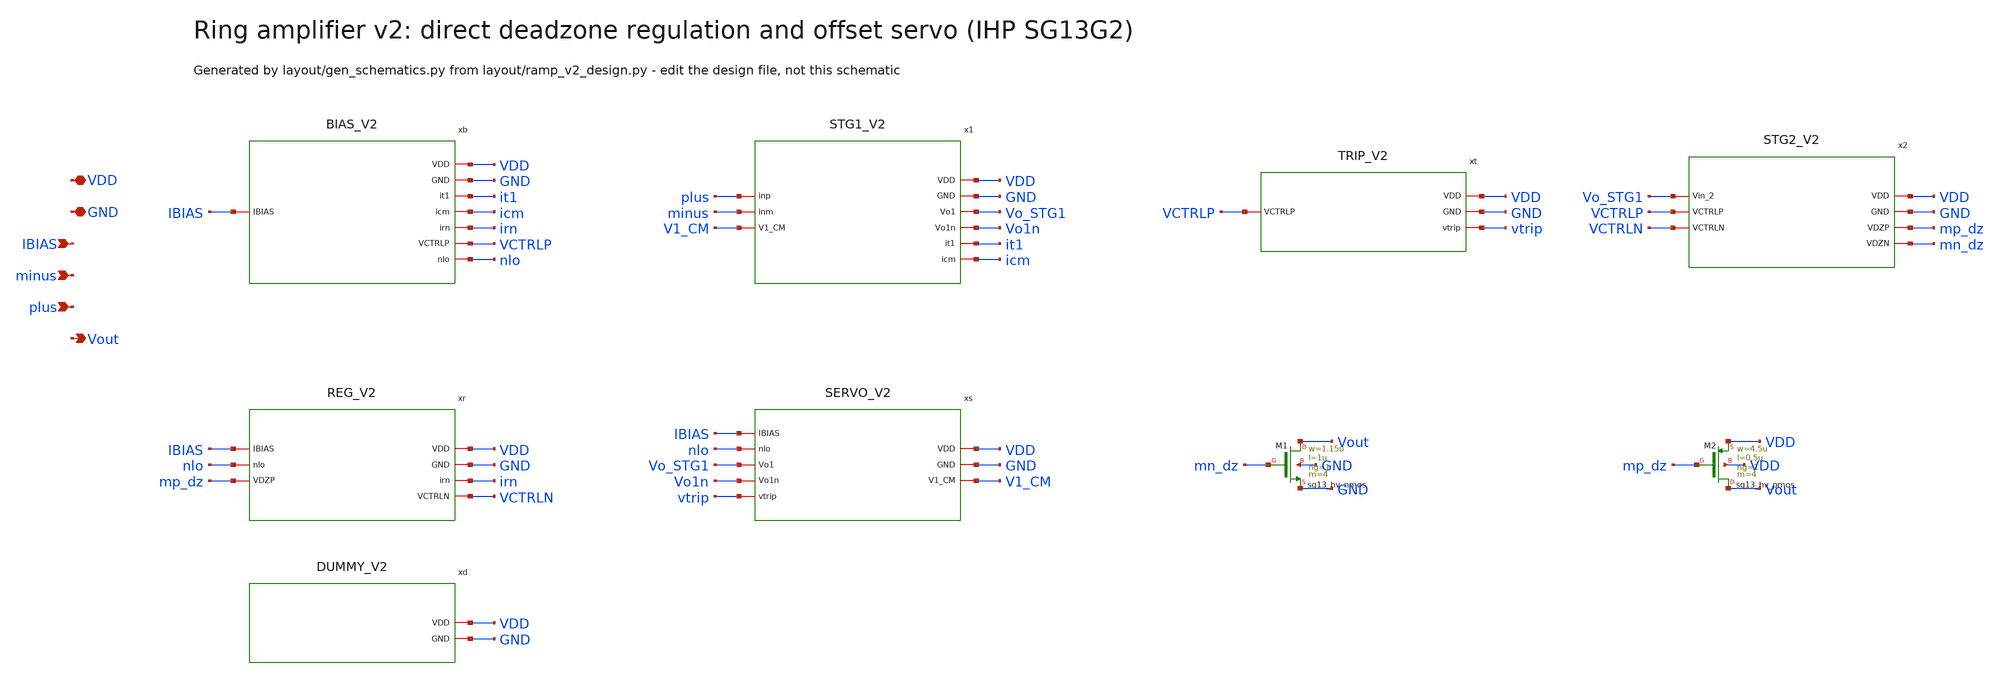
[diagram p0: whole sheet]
** sch_path: Design Files/RAMP/RAMP-V2/RAMP_V2.sch
**.subckt RAMP_V2 VDD GND IBIAS minus plus Vout
*.iopin VDD
*.iopin GND
*.ipin IBIAS
*.ipin minus
*.ipin plus
*.opin Vout
xb VDD GND IBIAS it1 icm irn VCTRLP nlo BIAS_V2
x1 VDD GND plus minus Vo_STG1 Vo1n V1_CM it1 icm STG1_V2
xt VDD GND VCTRLP vtrip TRIP_V2
x2 VDD GND Vo_STG1 VCTRLP VCTRLN mp_dz mn_dz STG2_V2
xr VDD GND IBIAS nlo mp_dz irn VCTRLN REG_V2
xs VDD GND IBIAS nlo Vo_STG1 Vo1n vtrip V1_CM SERVO_V2
XM1 Vout mn_dz GND GND sg13_hv_nmos w=1.15u l=1u ng=1 m=4 mm_ok=1
XM2 Vout mp_dz VDD VDD sg13_hv_pmos w=4.5u l=0.5u ng=1 m=4 mm_ok=1
xd VDD GND DUMMY_V2
**.ends

* expanding   symbol:  RAMP-V2/BIAS_V2.sym # of pins=8
** sym_path: Design Files/RAMP/RAMP-V2/BIAS_V2.sym
** sch_path: Design Files/RAMP/RAMP-V2/BIAS_V2.sch
.subckt BIAS_V2 VDD GND IBIAS it1 icm irn VCTRLP nlo
*.iopin VDD
*.iopin GND
*.ipin IBIAS
*.opin it1
*.opin icm
*.opin irn
*.opin VCTRLP
*.opin nlo
XMB0 IBIAS IBIAS GND GND sg13_lv_nmos w=0.5u l=8u ng=1 m=1 mm_ok=1
XMB2 pb IBIAS GND GND sg13_lv_nmos w=0.5u l=8u ng=1 m=2 mm_ok=1
XMB4 irn IBIAS GND GND sg13_lv_nmos w=0.5u l=8u ng=1 m=2 mm_ok=1
XMB5 VCTRLP IBIAS GND GND sg13_lv_nmos w=0.5u l=8u ng=1 m=3 mm_ok=1
XMBL0 plo IBIAS GND GND sg13_lv_nmos w=0.5u l=8u ng=1 m=1 mm_ok=1
XMBP0 pb pb VDD VDD sg13_lv_pmos w=4u l=1u ng=1 m=1 mm_ok=1
XMBP1 it1 pb VDD VDD sg13_lv_pmos w=4u l=1u ng=1 m=20 mm_ok=1
XMBP2 icm pb VDD VDD sg13_lv_pmos w=4u l=1u ng=1 m=5 mm_ok=1
XMBL1 plo plo VDD VDD sg13_hv_pmos w=1u l=1u ng=1 m=13 mm_ok=1
XMBL2 nlo plo VDD VDD sg13_hv_pmos w=1u l=1u ng=1 m=1 mm_ok=1
XMBL3 nlo nlo GND GND sg13_hv_nmos w=0.3u l=2u ng=1 m=14 mm_ok=1
XMD VCTRLP VCTRLP VDD VDD sg13_lv_pmos w=0.15u l=0.13u ng=1 m=1 mm_ok=1
.ends


* expanding   symbol:  RAMP-V2/STG1_V2.sym # of pins=9
** sym_path: Design Files/RAMP/RAMP-V2/STG1_V2.sym
** sch_path: Design Files/RAMP/RAMP-V2/STG1_V2.sch
.subckt STG1_V2 VDD GND inp inm Vo1 Vo1n V1_CM it1 icm
*.iopin VDD
*.iopin GND
*.ipin inp
*.ipin inm
*.opin Vo1
*.opin Vo1n
*.ipin V1_CM
*.iopin it1
*.iopin icm
XMN1 Vo1n inm it1 VDD sg13_lv_pmos w=2.5u l=0.5u ng=1 m=16 mm_ok=1
XMN2 Vo1 inp it1 VDD sg13_lv_pmos w=2.5u l=0.5u ng=1 m=16 mm_ok=1
XMP1 Vo1n vcmfb GND GND sg13_lv_nmos w=1u l=2u ng=1 m=4 mm_ok=1
XMP2 Vo1 vcmfb GND GND sg13_lv_nmos w=1u l=2u ng=1 m=4 mm_ok=1
XR1 Vo1n net3 GND rhigh w=0.5e-6 l=5.73e-6 m=1 b=0 mm_ok=1
XR3 Vo1 net3 GND rhigh w=0.5e-6 l=5.73e-6 m=1 b=0 mm_ok=1
XMC1 vcmfb V1_CM icm VDD sg13_lv_pmos w=2u l=1u ng=1 m=2 mm_ok=1
XMC2 dB net3 icm VDD sg13_lv_pmos w=2u l=1u ng=1 m=2 mm_ok=1
XMPC1 vcmfb vcmfb GND GND sg13_lv_nmos w=1u l=2u ng=1 m=1 mm_ok=1
XMPC2 dB dB GND GND sg13_lv_nmos w=1u l=2u ng=1 m=1 mm_ok=1
.ends


* expanding   symbol:  RAMP-V2/TRIP_V2.sym # of pins=4
** sym_path: Design Files/RAMP/RAMP-V2/TRIP_V2.sym
** sch_path: Design Files/RAMP/RAMP-V2/TRIP_V2.sch
.subckt TRIP_V2 VDD GND VCTRLP vtrip
*.iopin VDD
*.iopin GND
*.ipin VCTRLP
*.opin vtrip
XMT1 vtrip vtrip GND GND sg13_lv_nmos w=0.15u l=0.13u ng=1 m=1 mm_ok=1
XMT2 vtrip vtrip ntr VDD sg13_lv_pmos w=0.15u l=0.13u ng=1 m=3 mm_ok=1
XMT3 ntr VCTRLP VDD VDD sg13_lv_pmos w=0.15u l=0.13u ng=1 m=5 mm_ok=1
.ends


* expanding   symbol:  RAMP-V2/STG2_V2.sym # of pins=7
** sym_path: Design Files/RAMP/RAMP-V2/STG2_V2.sym
** sch_path: Design Files/RAMP/RAMP-V2/STG2_V2.sch
.subckt STG2_V2 VDD GND Vin_2 VCTRLP VCTRLN VDZP VDZN
*.iopin VDD
*.iopin GND
*.ipin Vin_2
*.ipin VCTRLP
*.ipin VCTRLN
*.opin VDZP
*.opin VDZN
XMN_STG2_3N1 VDZN Vin_2 GND GND sg13_lv_nmos w=0.15u l=0.13u ng=1 m=3 mm_ok=1
XMN_STG2_3P1 VDZN Vin_2 n2a VDD sg13_lv_pmos w=0.15u l=0.13u ng=1 m=9 mm_ok=1
XMP_DZ_STG2_3N n2a VCTRLP VDD VDD sg13_lv_pmos w=0.15u l=0.13u ng=1 m=15 mm_ok=1
XMP_STG2_3P2 VDZP Vin_2 n2b GND sg13_lv_nmos w=0.15u l=0.13u ng=1 m=6 mm_ok=1
XMP_STG2_3P1 VDZP Vin_2 VDD VDD sg13_lv_pmos w=0.15u l=0.13u ng=1 m=1 mm_ok=1
XMN_DZ_STG2_3P n2b VCTRLN GND GND sg13_lv_nmos w=0.15u l=0.3u ng=1 m=6 mm_ok=1
.ends


* expanding   symbol:  RAMP-V2/REG_V2.sym # of pins=7
** sym_path: Design Files/RAMP/RAMP-V2/REG_V2.sym
** sch_path: Design Files/RAMP/RAMP-V2/REG_V2.sch
.subckt REG_V2 VDD GND IBIAS nlo VDZP irn VCTRLN
*.iopin VDD
*.iopin GND
*.ipin IBIAS
*.ipin nlo
*.ipin VDZP
*.iopin irn
*.opin VCTRLN
XMPR irn irn VDD VDD sg13_hv_pmos w=4.5u l=0.5u ng=1 m=2 mm_ok=1
XRS VDZP vgps GND rhigh w=0.5e-6 l=171.9e-6 m=1 b=0 mm_ok=1
XM1 d1 irn t GND sg13_hv_nmos w=4u l=4u ng=1 m=1 mm_ok=1
XM2 o1 vgps t GND sg13_hv_nmos w=4u l=4u ng=1 m=1 mm_ok=1
XM3 d1 d1 VDD VDD sg13_hv_pmos w=1u l=2u ng=1 m=1 mm_ok=1
XM4 o1 d1 VDD VDD sg13_hv_pmos w=1u l=2u ng=1 m=1 mm_ok=1
XM5a t nlo s1 GND sg13_hv_nmos w=0.3u l=2u ng=1 m=1 mm_ok=1
XM5b s1 nlo s2 GND sg13_hv_nmos w=0.3u l=2u ng=1 m=1 mm_ok=1
XM5c s2 nlo s3 GND sg13_hv_nmos w=0.3u l=2u ng=1 m=1 mm_ok=1
XM5d s3 nlo s4 GND sg13_hv_nmos w=0.3u l=2u ng=1 m=1 mm_ok=1
XM5e s4 nlo s5 GND sg13_hv_nmos w=0.3u l=2u ng=1 m=1 mm_ok=1
XM5f s5 nlo GND GND sg13_hv_nmos w=0.3u l=2u ng=1 m=1 mm_ok=1
XM6 VCTRLN o1 VDD VDD sg13_hv_pmos w=1u l=1u ng=1 m=1 mm_ok=1
XM7 VCTRLN IBIAS GND GND sg13_lv_nmos w=0.5u l=8u ng=1 m=1 mm_ok=1
XRZ VCTRLN z GND rhigh w=0.5e-6 l=11.46e-6 m=1 b=0 mm_ok=1
XCC o1 z cap_cmim w=51.6e-6 l=51.6e-6 m=1 mm_ok=1
.ends


* expanding   symbol:  RAMP-V2/SERVO_V2.sym # of pins=8
** sym_path: Design Files/RAMP/RAMP-V2/SERVO_V2.sym
** sch_path: Design Files/RAMP/RAMP-V2/SERVO_V2.sch
.subckt SERVO_V2 VDD GND IBIAS nlo Vo1 Vo1n vtrip V1_CM
*.iopin VDD
*.iopin GND
*.ipin IBIAS
*.ipin nlo
*.ipin Vo1
*.ipin Vo1n
*.ipin vtrip
*.opin V1_CM
XM1 d1 Vo1n t GND sg13_hv_nmos w=3u l=3u ng=1 m=1 mm_ok=1
XM2 o1 Vo1 t GND sg13_hv_nmos w=3u l=3u ng=1 m=1 mm_ok=1
XM3 d1 d1 VDD VDD sg13_hv_pmos w=1u l=2u ng=1 m=1 mm_ok=1
XM4 o1 d1 VDD VDD sg13_hv_pmos w=1u l=2u ng=1 m=1 mm_ok=1
XM5a t nlo s1 GND sg13_hv_nmos w=0.3u l=2u ng=1 m=1 mm_ok=1
XM5b s1 nlo s2 GND sg13_hv_nmos w=0.3u l=2u ng=1 m=1 mm_ok=1
XM5c s2 nlo GND GND sg13_hv_nmos w=0.3u l=2u ng=1 m=1 mm_ok=1
XM6 VSV o1 VDD VDD sg13_hv_pmos w=1u l=1u ng=1 m=1 mm_ok=1
XM7 VSV IBIAS GND GND sg13_lv_nmos w=0.5u l=8u ng=1 m=1 mm_ok=1
XRZ VSV z GND rhigh w=0.5e-6 l=11.46e-6 m=1 b=0 mm_ok=1
XCC o1 z cap_cmim w=25.8e-6 l=25.8e-6 m=1 mm_ok=1
XRTA VSV V1_CM GND rhigh w=0.5e-6 l=171.9e-6 m=1 b=0 mm_ok=1
XRTB vtrip V1_CM GND rhigh w=0.5e-6 l=22.92e-6 m=1 b=0 mm_ok=1
.ends


* expanding   symbol:  RAMP-V2/DUMMY_V2.sym # of pins=2
** sym_path: Design Files/RAMP/RAMP-V2/DUMMY_V2.sym
** sch_path: Design Files/RAMP/RAMP-V2/DUMMY_V2.sch
.subckt DUMMY_V2 VDD GND
*.iopin VDD
*.iopin GND
XMD0 GND GND GND GND sg13_hv_nmos w=0.3u l=2u ng=1 m=4 mm_ok=1
XMD1 GND GND GND GND sg13_hv_nmos w=1.15u l=1u ng=1 m=2 mm_ok=1
XMD2 GND GND GND GND sg13_hv_nmos w=3u l=3u ng=1 m=2 mm_ok=1
XMD3 GND GND GND GND sg13_hv_nmos w=4u l=4u ng=1 m=2 mm_ok=1
XMD4 GND GND GND GND sg13_lv_nmos w=0.15u l=0.13u ng=1 m=4 mm_ok=1
XMD5 GND GND GND GND sg13_lv_nmos w=0.15u l=0.3u ng=1 m=2 mm_ok=1
XMD6 GND GND GND GND sg13_lv_nmos w=0.5u l=8u ng=1 m=5 mm_ok=1
XMD7 GND GND GND GND sg13_lv_nmos w=1u l=2u ng=1 m=3 mm_ok=1
XMD8 VDD VDD VDD VDD sg13_hv_pmos w=1u l=1u ng=1 m=2 mm_ok=1
XMD9 VDD VDD VDD VDD sg13_hv_pmos w=1u l=2u ng=1 m=2 mm_ok=1
XMD10 VDD VDD VDD VDD sg13_hv_pmos w=4.5u l=0.5u ng=1 m=2 mm_ok=1
XMD11 VDD VDD VDD VDD sg13_lv_pmos w=0.15u l=0.13u ng=1 m=4 mm_ok=1
XMD12 VDD VDD VDD VDD sg13_lv_pmos w=2u l=1u ng=1 m=2 mm_ok=1
XMD13 VDD VDD VDD VDD sg13_lv_pmos w=2.5u l=0.5u ng=1 m=2 mm_ok=1
XMD14 VDD VDD VDD VDD sg13_lv_pmos w=4u l=1u ng=1 m=2 mm_ok=1
.ends

.end
